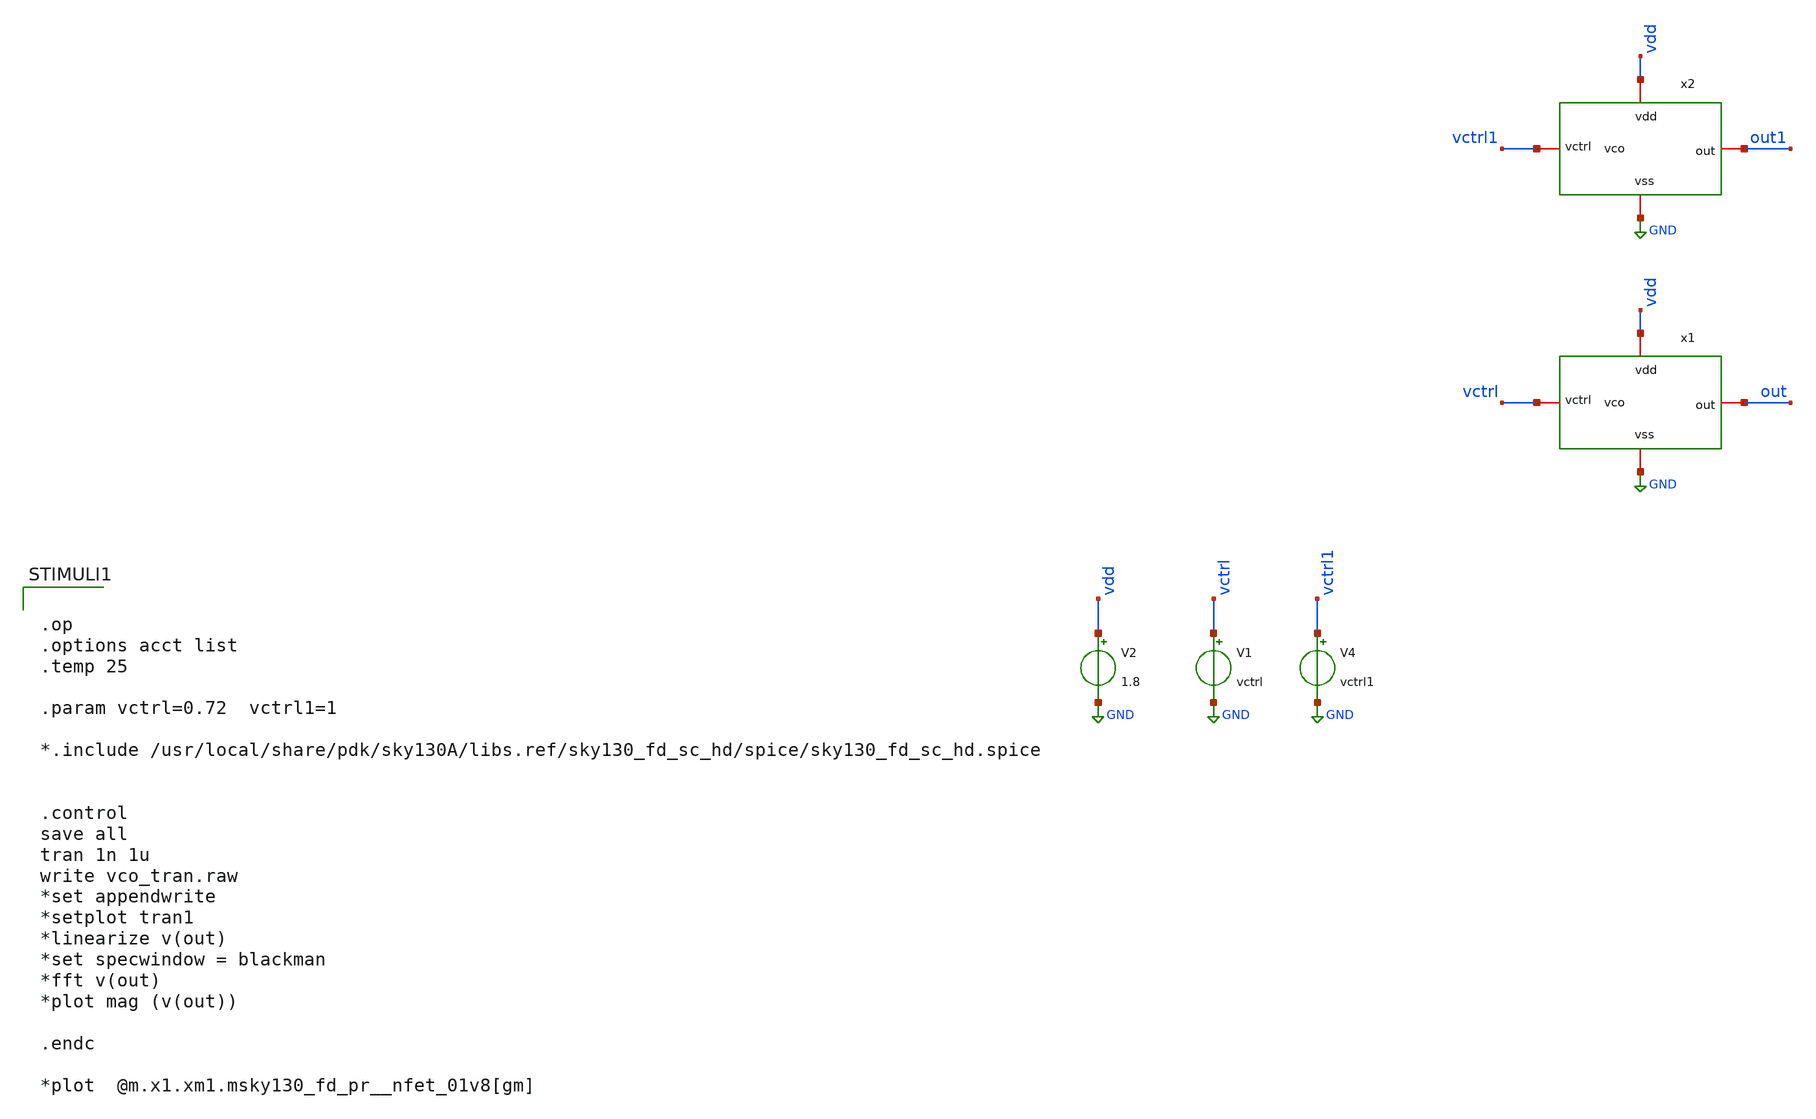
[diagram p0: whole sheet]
** sch_path: xschem/vco/vco_tran.sch
**.subckt vco_tran
x1 vdd out vctrl GND vco
V1 vctrl GND vctrl
V2 vdd GND 1.8
x2 vdd out1 vctrl1 GND vco
V4 vctrl1 GND vctrl1
**** begin user architecture code

** opencircuitdesign pdks install
.lib $::SKYWATER_MODELS/sky130.lib.spice tt




.op
.options acct list
.temp 25

.param vctrl=0.72  vctrl1=1

*.include /usr/local/share/pdk/sky130A/libs.ref/sky130_fd_sc_hd/spice/sky130_fd_sc_hd.spice


.control
save all
tran 1n 1u
write vco_tran.raw
*set appendwrite
*setplot tran1
*linearize v(out)
*set specwindow = blackman
*fft v(out)
*plot mag (v(out))

.endc

*plot  @m.x1.xm1.msky130_fd_pr__nfet_01v8[gm]


**** end user architecture code
**.ends

* expanding   symbol:  vco/vco.sym # of pins=4
** sym_path: xschem01/vco/vco.sym
** sch_path: xschem01/vco/vco.sch
.subckt vco vdd out vctrl vss
*.iopin vdd
*.iopin vss
*.iopin out
*.iopin vctrl
XM1 net1 vctrl vss vss sky130_fd_pr__nfet_01v8 L=0.15 W=30 nf=1 ad='int((nf+1)/2) * W/nf * 0.29' as='int((nf+2)/2) * W/nf * 0.29'
+ pd='2*int((nf+1)/2) * (W/nf + 0.29)' ps='2*int((nf+2)/2) * (W/nf + 0.29)' nrd='0.29 / W' nrs='0.29 / W'
+ sa=0 sb=0 sd=0 mult=1 m=1
XM2 net1 net1 vdd vdd sky130_fd_pr__pfet_01v8 L=0.15 W=90 nf=1 ad='int((nf+1)/2) * W/nf * 0.29' as='int((nf+2)/2) * W/nf * 0.29'
+ pd='2*int((nf+1)/2) * (W/nf + 0.29)' ps='2*int((nf+2)/2) * (W/nf + 0.29)' nrd='0.29 / W' nrs='0.29 / W'
+ sa=0 sb=0 sd=0 mult=1 m=1
XM3 net4 net1 vdd vdd sky130_fd_pr__pfet_01v8 L=0.15 W=80 nf=1 ad='int((nf+1)/2) * W/nf * 0.29' as='int((nf+2)/2) * W/nf * 0.29'
+ pd='2*int((nf+1)/2) * (W/nf + 0.29)' ps='2*int((nf+2)/2) * (W/nf + 0.29)' nrd='0.29 / W' nrs='0.29 / W'
+ sa=0 sb=0 sd=0 mult=1 m=1
XM4 net3 out net4 net4 sky130_fd_pr__pfet_01v8 L=0.15 W=80 nf=1 ad='int((nf+1)/2) * W/nf * 0.29' as='int((nf+2)/2) * W/nf * 0.29'
+ pd='2*int((nf+1)/2) * (W/nf + 0.29)' ps='2*int((nf+2)/2) * (W/nf + 0.29)' nrd='0.29 / W' nrs='0.29 / W'
+ sa=0 sb=0 sd=0 mult=1 m=1
XM5 net2 vctrl vss vss sky130_fd_pr__nfet_01v8 L=0.15 W=30 nf=1 ad='int((nf+1)/2) * W/nf * 0.29' as='int((nf+2)/2) * W/nf * 0.29'
+ pd='2*int((nf+1)/2) * (W/nf + 0.29)' ps='2*int((nf+2)/2) * (W/nf + 0.29)' nrd='0.29 / W' nrs='0.29 / W'
+ sa=0 sb=0 sd=0 mult=1 m=1
XM6 net3 out net2 vss sky130_fd_pr__nfet_01v8 L=0.15 W=30 nf=1 ad='int((nf+1)/2) * W/nf * 0.29' as='int((nf+2)/2) * W/nf * 0.29'
+ pd='2*int((nf+1)/2) * (W/nf + 0.29)' ps='2*int((nf+2)/2) * (W/nf + 0.29)' nrd='0.29 / W' nrs='0.29 / W'
+ sa=0 sb=0 sd=0 mult=1 m=1
XM7 net7 net1 vdd vdd sky130_fd_pr__pfet_01v8 L=0.15 W=80 nf=1 ad='int((nf+1)/2) * W/nf * 0.29' as='int((nf+2)/2) * W/nf * 0.29'
+ pd='2*int((nf+1)/2) * (W/nf + 0.29)' ps='2*int((nf+2)/2) * (W/nf + 0.29)' nrd='0.29 / W' nrs='0.29 / W'
+ sa=0 sb=0 sd=0 mult=2 m=2
XM8 net6 net3 net7 net7 sky130_fd_pr__pfet_01v8 L=0.15 W=80 nf=1 ad='int((nf+1)/2) * W/nf * 0.29' as='int((nf+2)/2) * W/nf * 0.29'
+ pd='2*int((nf+1)/2) * (W/nf + 0.29)' ps='2*int((nf+2)/2) * (W/nf + 0.29)' nrd='0.29 / W' nrs='0.29 / W'
+ sa=0 sb=0 sd=0 mult=2 m=2
XM9 net5 vctrl vss vss sky130_fd_pr__nfet_01v8 L=0.15 W=60 nf=1 ad='int((nf+1)/2) * W/nf * 0.29' as='int((nf+2)/2) * W/nf * 0.29'
+ pd='2*int((nf+1)/2) * (W/nf + 0.29)' ps='2*int((nf+2)/2) * (W/nf + 0.29)' nrd='0.29 / W' nrs='0.29 / W'
+ sa=0 sb=0 sd=0 mult=1 m=1
XM10 net6 net3 net5 vss sky130_fd_pr__nfet_01v8 L=0.15 W=60 nf=1 ad='int((nf+1)/2) * W/nf * 0.29' as='int((nf+2)/2) * W/nf * 0.29'
+ pd='2*int((nf+1)/2) * (W/nf + 0.29)' ps='2*int((nf+2)/2) * (W/nf + 0.29)' nrd='0.29 / W' nrs='0.29 / W'
+ sa=0 sb=0 sd=0 mult=1 m=1
XM11 net9 net1 vdd vdd sky130_fd_pr__pfet_01v8 L=0.15 W=80 nf=1 ad='int((nf+1)/2) * W/nf * 0.29' as='int((nf+2)/2) * W/nf * 0.29'
+ pd='2*int((nf+1)/2) * (W/nf + 0.29)' ps='2*int((nf+2)/2) * (W/nf + 0.29)' nrd='0.29 / W' nrs='0.29 / W'
+ sa=0 sb=0 sd=0 mult=3 m=3
XM12 out net6 net9 net9 sky130_fd_pr__pfet_01v8 L=0.15 W=80 nf=1 ad='int((nf+1)/2) * W/nf * 0.29' as='int((nf+2)/2) * W/nf * 0.29'
+ pd='2*int((nf+1)/2) * (W/nf + 0.29)' ps='2*int((nf+2)/2) * (W/nf + 0.29)' nrd='0.29 / W' nrs='0.29 / W'
+ sa=0 sb=0 sd=0 mult=3 m=3
XM13 net8 vctrl vss vss sky130_fd_pr__nfet_01v8 L=0.15 W=90 nf=1 ad='int((nf+1)/2) * W/nf * 0.29' as='int((nf+2)/2) * W/nf * 0.29'
+ pd='2*int((nf+1)/2) * (W/nf + 0.29)' ps='2*int((nf+2)/2) * (W/nf + 0.29)' nrd='0.29 / W' nrs='0.29 / W'
+ sa=0 sb=0 sd=0 mult=1 m=1
XM14 out net6 net8 vss sky130_fd_pr__nfet_01v8 L=0.15 W=90 nf=1 ad='int((nf+1)/2) * W/nf * 0.29' as='int((nf+2)/2) * W/nf * 0.29'
+ pd='2*int((nf+1)/2) * (W/nf + 0.29)' ps='2*int((nf+2)/2) * (W/nf + 0.29)' nrd='0.29 / W' nrs='0.29 / W'
+ sa=0 sb=0 sd=0 mult=1 m=1
.ends

.GLOBAL GND
.end
